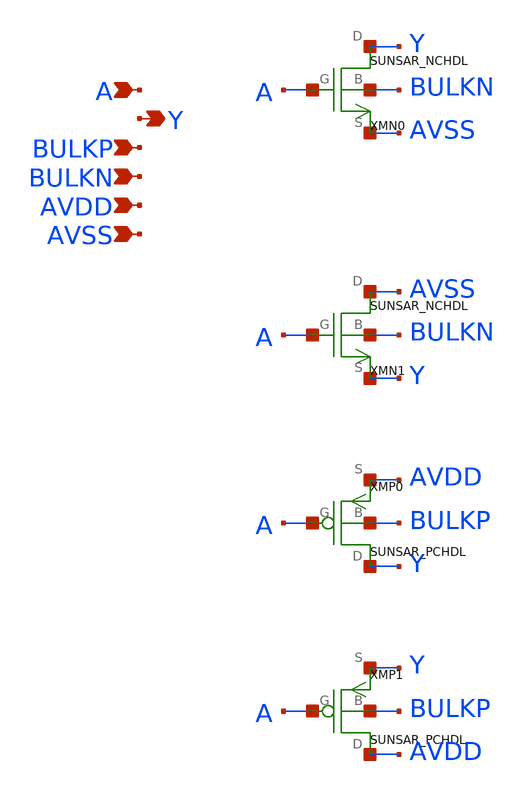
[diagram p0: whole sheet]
** sch_path: design/SUN_SAR9B_SKY130NM/SUNSAR_IVX2_CV.sch
**.subckt SUNSAR_IVX2_CV A Y BULKP BULKN AVDD AVSS
*.ipin A
*.opin Y
*.ipin BULKP
*.ipin BULKN
*.ipin AVDD
*.ipin AVSS
XMN0 Y A AVSS BULKN SUNSAR_NCHDL
XMN1 AVSS A Y BULKN SUNSAR_NCHDL
XMP0 Y A AVDD BULKP SUNSAR_PCHDL
XMP1 AVDD A Y BULKP SUNSAR_PCHDL
**.ends
.end
